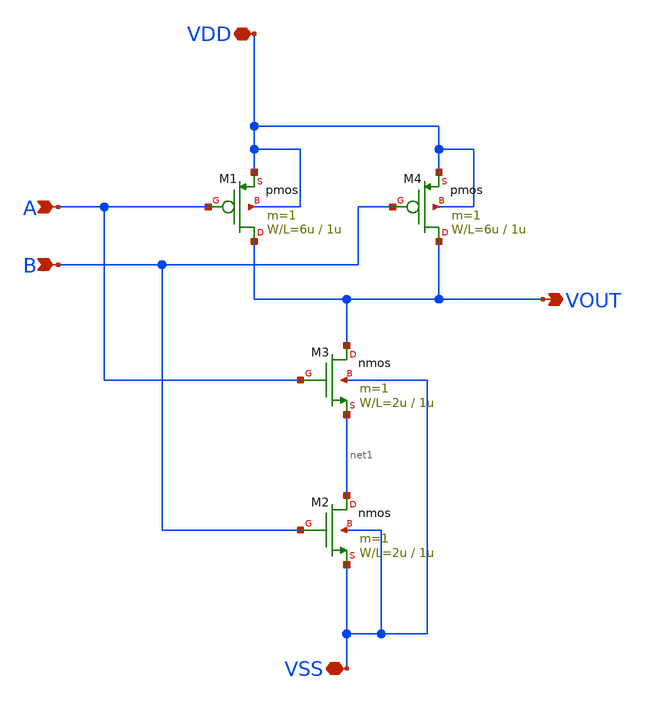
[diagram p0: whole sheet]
** sch_path: member_project/sanken/shishido/NAND/NAND.sch
**.subckt NAND VDD VSS VOUT A B
*.iopin VDD
*.iopin VSS
*.opin VOUT
*.ipin A
*.ipin B
M2 net1 B VSS VSS nmos L=1u W=2u m=1
M1 VOUT A VDD VDD pmos L=1u W=6u m=1
M3 VOUT A net1 VSS nmos L=1u W=2u m=1
M4 VOUT B VDD VDD pmos L=1u W=6u m=1
**.ends
.end
